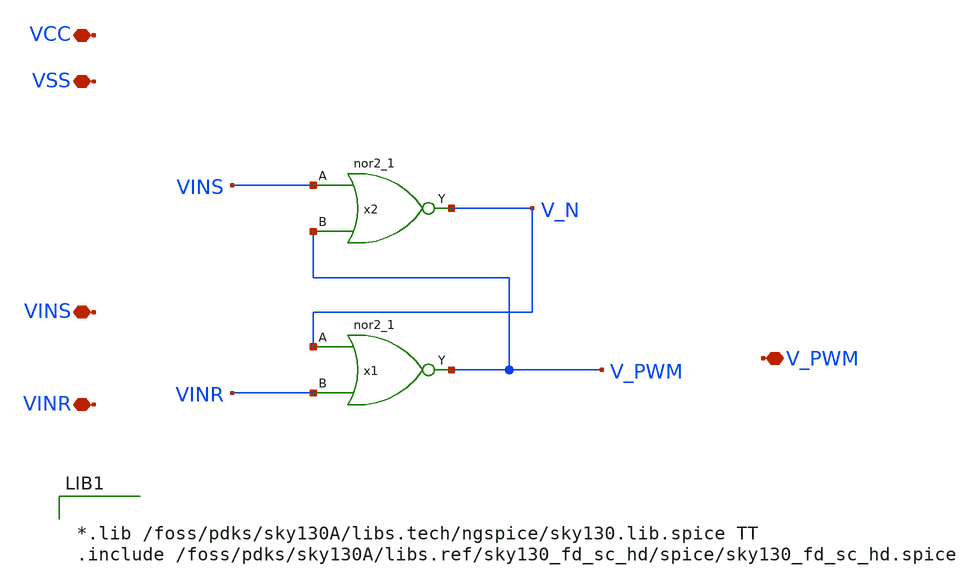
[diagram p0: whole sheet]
** sch_path: xschem/SRlatch_NOR.sch
**.subckt SRlatch_NOR VINS V_PWM VCC VSS VINR
*.iopin VINS
*.iopin V_PWM
*.iopin VCC
*.iopin VSS
*.iopin VINR
x2 VINS V_PWM VSS VSS VCC VCC V_N sky130_fd_sc_hd__nor2_1
x1 V_N VINR VSS VSS VCC VCC V_PWM sky130_fd_sc_hd__nor2_1
**** begin user architecture code


*.lib /foss/pdks/sky130A/libs.tech/ngspice/sky130.lib.spice TT
.include /foss/pdks/sky130A/libs.ref/sky130_fd_sc_hd/spice/sky130_fd_sc_hd.spice


**** end user architecture code
**.ends
.end
